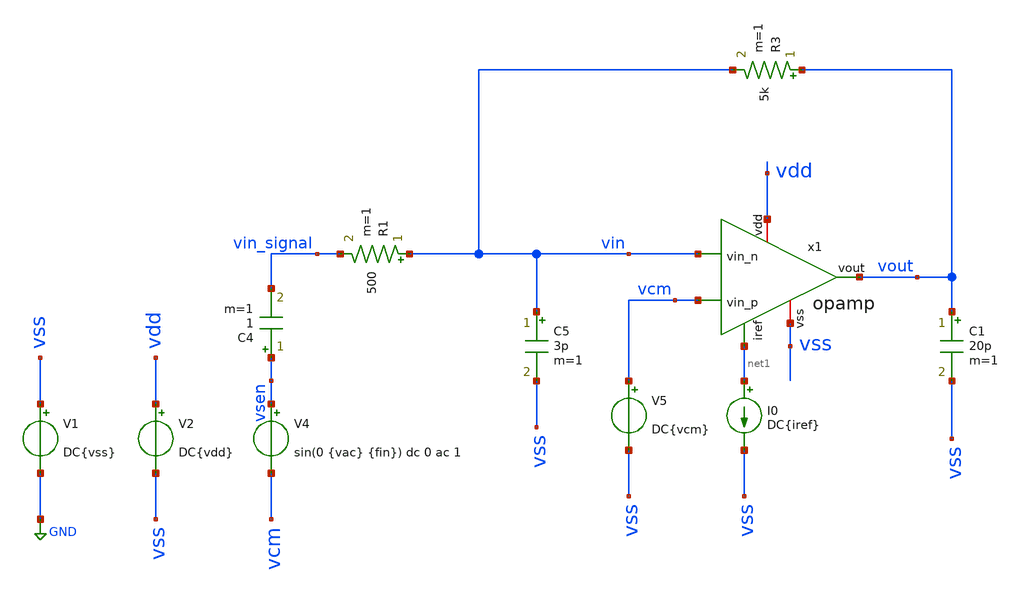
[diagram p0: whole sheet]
** sch_path: TpFinal/Mis Simulaciones/tb_opamp_closeloop.sch
**.subckt tb_opamp_closeloop
V1 vss GND DC{vss}
V2 vdd vss DC{vdd}
V4 vsen vcm sin(0 {vac} {fin}) dc 0 ac 1
C4 vsen vin_signal 1 m=1
I0 net1 vss DC{iref}
R1 vin vin_signal 500 m=1
R3 vout vin 5k m=1
C5 vin vss 3p m=1
C1 vout vss 20p m=1
V5 vcm vss DC{vcm}
x1 vdd net1 vin vcm vout vss opamp
**** begin user architecture code




* Circuit Parameters
.param iref = 105u
.param vdd  = 1.98
.param vss  = 0.0
.param vcm  = 0.88
.param vac  = 10m
.param fin  = 9.765625e5
.options TEMP = 0.0

* FFT Parameters
.param Ts_FFT     = 1e-9
.csparam Ts_FFT   = {Ts_FFT}
.param fin_approx = 1e6
.param NFFT       = 4096
.csparam NFFT     = {NFFT}
.param vac_fin    = 'floor(fin_approx*Ts_FFT*NFFT)/Ts_FFT/NFFT'
.csparam Ti_FFT   = 3u
.csparam vac_fin  = {vac_fin}

* Include Models
.lib ~/skywater/skywater-pdk/libraries/sky130_fd_pr_ngspice/latest/models/corners/sky130.lib FF

* OP Parameters & Singals to save
.save all  @M.X1.XM1.msky130_fd_pr__pfet_01v8_lvt[id] @M.X1.XM1.msky130_fd_pr__pfet_01v8_lvt[vth] @M.X1.XM1.msky130_fd_pr__pfet_01v8_lvt[vgs] @M.X1.XM1.msky130_fd_pr__pfet_01v8_lvt[vds] @M.X1.XM1.msky130_fd_pr__pfet_01v8_lvt[vdsat] @M.X1.XM1.msky130_fd_pr__pfet_01v8_lvt[gm] @M.X1.XM1.msky130_fd_pr__pfet_01v8_lvt[gds] @M.X1.XM1.msky130_fd_pr__pfet_01v8_lvt[cgg]  @M.X1.XM2.msky130_fd_pr__pfet_01v8_lvt[id] @M.X1.XM2.msky130_fd_pr__pfet_01v8_lvt[vth] @M.X1.XM2.msky130_fd_pr__pfet_01v8_lvt[vgs] @M.X1.XM2.msky130_fd_pr__pfet_01v8_lvt[vds] @M.X1.XM2.msky130_fd_pr__pfet_01v8_lvt[vdsat] @M.X1.XM2.msky130_fd_pr__pfet_01v8_lvt[gm] @M.X1.XM2.msky130_fd_pr__pfet_01v8_lvt[gds] @M.X1.XM2.msky130_fd_pr__pfet_01v8_lvt[cgg]  @M.X1.XM3.msky130_fd_pr__nfet_01v8[id] @M.X1.XM3.msky130_fd_pr__nfet_01v8[vth] @M.X1.XM3.msky130_fd_pr__nfet_01v8[vgs] @M.X1.XM3.msky130_fd_pr__nfet_01v8[vds] @M.X1.XM3.msky130_fd_pr__nfet_01v8[vdsat] @M.X1.XM3.msky130_fd_pr__nfet_01v8[gm] @M.X1.XM3.msky130_fd_pr__nfet_01v8[gds]  @M.X1.XM4.msky130_fd_pr__nfet_01v8[id] @M.X1.XM4.msky130_fd_pr__nfet_01v8[vth] @M.X1.XM4.msky130_fd_pr__nfet_01v8[vgs] @M.X1.XM4.msky130_fd_pr__nfet_01v8[vds] @M.X1.XM4.msky130_fd_pr__nfet_01v8[vdsat] @M.X1.XM4.msky130_fd_pr__nfet_01v8[gm] @M.X1.XM4.msky130_fd_pr__nfet_01v8[gds]  @M.X1.XM5.msky130_fd_pr__pfet_01v8[id] @M.X1.XM5.msky130_fd_pr__pfet_01v8[vth] @M.X1.XM5.msky130_fd_pr__pfet_01v8[vgs] @M.X1.XM5.msky130_fd_pr__pfet_01v8[vds] @M.X1.XM5.msky130_fd_pr__pfet_01v8[vdsat] @M.X1.XM5.msky130_fd_pr__pfet_01v8[gm] @M.X1.XM5.msky130_fd_pr__pfet_01v8[gds]  @M.X1.XM6.msky130_fd_pr__nfet_01v8[id] @M.X1.XM6.msky130_fd_pr__nfet_01v8[vth] @M.X1.XM6.msky130_fd_pr__nfet_01v8[vgs] @M.X1.XM6.msky130_fd_pr__nfet_01v8[vds] @M.X1.XM6.msky130_fd_pr__nfet_01v8[vdsat] @M.X1.XM6.msky130_fd_pr__nfet_01v8[gm] @M.X1.XM6.msky130_fd_pr__nfet_01v8[gds]  @M.X1.XM7.msky130_fd_pr__pfet_01v8[id] @M.X1.XM7.msky130_fd_pr__pfet_01v8[vth] @M.X1.XM7.msky130_fd_pr__pfet_01v8[vgs] @M.X1.XM7.msky130_fd_pr__pfet_01v8[vds] @M.X1.XM7.msky130_fd_pr__pfet_01v8[vdsat] @M.X1.XM7.msky130_fd_pr__pfet_01v8[gm] @M.X1.XM7.msky130_fd_pr__pfet_01v8[gds]  @M.X1.XM8.msky130_fd_pr__pfet_01v8[id] @M.X1.XM8.msky130_fd_pr__pfet_01v8[vth] @M.X1.XM8.msky130_fd_pr__pfet_01v8[vgs] @M.X1.XM8.msky130_fd_pr__pfet_01v8[vds] @M.X1.XM8.msky130_fd_pr__pfet_01v8[vdsat] @M.X1.XM8.msky130_fd_pr__pfet_01v8[gm] @M.X1.XM8.msky130_fd_pr__pfet_01v8[gds]  @M.X1.XM9.msky130_fd_pr__nfet_01v8[id] @M.X1.XM9.msky130_fd_pr__nfet_01v8[vth] @M.X1.XM9.msky130_fd_pr__nfet_01v8[vgs] @M.X1.XM9.msky130_fd_pr__nfet_01v8[vds] @M.X1.XM9.msky130_fd_pr__nfet_01v8[vdsat] @M.X1.XM9.msky130_fd_pr__nfet_01v8[gm] @M.X1.XM9.msky130_fd_pr__nfet_01v8[gds]

*Simulation
.control
  set color0 = white

  ac dec 100 1k 10G
  setplot ac1
  meas ac GBW when vdb(vout)=0
  meas ac DCG find vdb(vout) at=1k
  plot vdb(vout) {vp(vout)*180/PI}

  reset
  tran 0.01u 11u
  setplot tran1
  plot v(vsen) v(vout)

  *reset
  *set sqrnoise
  *noise v(vout) V4 dec 100 1k 10G 1
  *let onoise_total_integrado = maximum(sqrt(integ(onoise_spectrum)))
  *print onoise_total_integrado

  reset
  noise v(vout) V4 dec 100 1k 10G 1
  setplot noise1
  plot onoise_spectrum
  setplot noise2
  print inoise_total
  print onoise_total
  print onoise_total.m.x1.xm1.msky130_fd_pr__pfet_01v8_lvt.1overf
  print onoise_total.m.x1.xm1.msky130_fd_pr__pfet_01v8_lvt.id
  print onoise_total.m.x1.xm2.msky130_fd_pr__pfet_01v8_lvt.1overf
  print onoise_total.m.x1.xm2.msky130_fd_pr__pfet_01v8_lvt.id
  print onoise_total.m.x1.xm3.msky130_fd_pr__nfet_01v8.1overf
  print onoise_total.m.x1.xm3.msky130_fd_pr__nfet_01v8.id
  print onoise_total.m.x1.xm4.msky130_fd_pr__nfet_01v8.1overf
  print onoise_total.m.x1.xm4.msky130_fd_pr__nfet_01v8.id
  print onoise_total.m.x1.xm5.msky130_fd_pr__pfet_01v8.1overf
  print onoise_total.m.x1.xm5.msky130_fd_pr__pfet_01v8.id
  print onoise_total.m.x1.xm6.msky130_fd_pr__nfet_01v8.1overf
  print onoise_total.m.x1.xm6.msky130_fd_pr__nfet_01v8.id
  print onoise_total.m.x1.xm7.msky130_fd_pr__pfet_01v8.1overf
  print onoise_total.m.x1.xm7.msky130_fd_pr__pfet_01v8.id
  vprint onoise_total.m.x1.xm8.msky130_fd_pr__pfet_01v8.1overf
  print onoise_total.m.x1.xm8.msky130_fd_pr__pfet_01v8.id
  set filetype=ascii
  write tpfinal_noise.raw

  reset
  set sqrnoise
  noise v(vout) V4 dec 100 1k 10G 1
  setplot noise3
  plot onoise_spectrum
  plot sqrt(integ(onoise_spectrum))
  let onoise_total_integrado = maximum(sqrt(integ(onoise_spectrum)))
  print onoise_total_integrado

  reset
  tran 0.001u 11u
  fourier 9.765625e5 vout
  let THD_db = db(fourier11[1][3]/fourier11[1][1])
  print THD_db
  let lin-tstart = {Ti_FFT} $ skip the start - up phase
  let lin-tstep = {Ts_FFT}
  let lin-tstop = {Ti_FFT + (NFFT-1) * Ts_FFT} $ end earlier
  linearize vout
  set specwindow = none
  fft vout
  *plot mag(vout)
  plot db(mag(vout)) xlimit 0 20e6

  reset
  op
  setplot op1
  unset filetype
  write tb_opamp_closeloop.raw
.endc

.end


**** end user architecture code
**.ends

* expanding   symbol:  opamp.sym # of pins=6
** sym_path: opamp.sym
** sch_path: opamp.sch
.subckt opamp vdd iref vin_n vin_p vout vss
*.iopin vdd
*.iopin vss
*.ipin vin_n
*.ipin vin_p
*.ipin iref
*.opin vout
XM3 vbn vbn vss vss sky130_fd_pr__nfet_01v8 L=3.6 W=40 nf=1 ad='W * 0.29' as='W * 0.29' pd='2 * (W + 0.29)'
+ ps='2 * (W + 0.29)' nrd='0.29 / W' nrs='0.29 / W' sa=0 sb=0 sd=0 mult=17 m=17
XM4 voe1 vbn vss vss sky130_fd_pr__nfet_01v8 L=3.6 W=40 nf=1 ad='W * 0.29' as='W * 0.29' pd='2 * (W + 0.29)'
+ ps='2 * (W + 0.29)' nrd='0.29 / W' nrs='0.29 / W' sa=0 sb=0 sd=0 mult=17 m=17
XM5 vp iref vdd vdd sky130_fd_pr__pfet_01v8 L=0.8 W=60 nf=1 ad='W * 0.29' as='W * 0.29' pd='2 * (W + 0.29)'
+ ps='2 * (W + 0.29)' nrd='0.29 / W' nrs='0.29 / W' sa=0 sb=0 sd=0 mult=54 m=54
XM7 vout iref vdd vdd sky130_fd_pr__pfet_01v8 L=0.8 W=60 nf=1 ad='W * 0.29' as='W * 0.29' pd='2 * (W + 0.29)'
+ ps='2 * (W + 0.29)' nrd='0.29 / W' nrs='0.29 / W' sa=0 sb=0 sd=0 mult=68 m=68
XM8 iref iref vdd vdd sky130_fd_pr__pfet_01v8 L=0.8 W=60 nf=1 ad='W * 0.29' as='W * 0.29' pd='2 * (W + 0.29)'
+ ps='2 * (W + 0.29)' nrd='0.29 / W' nrs='0.29 / W' sa=0 sb=0 sd=0 mult=5 m=5
XM9 net1 vdd voe1 vss sky130_fd_pr__nfet_01v8 L=0.15 W=8.1 nf=1 ad='W * 0.29' as='W * 0.29' pd='2 * (W + 0.29)'
+ ps='2 * (W + 0.29)' nrd='0.29 / W' nrs='0.29 / W' sa=0 sb=0 sd=0 mult=1 m=1
XM6 vout voe1 vss vss sky130_fd_pr__nfet_01v8 L=0.16 W=82 nf=1 ad='W * 0.29' as='W * 0.29' pd='2 * (W + 0.29)'
+ ps='2 * (W + 0.29)' nrd='0.29 / W' nrs='0.29 / W' sa=0 sb=0 sd=0 mult=14 m=14
XM1 vbn vin_n vp vp sky130_fd_pr__pfet_01v8_lvt L=0.5 W=45 nf=1 ad='int((nf+1)/2) * W/nf * 0.29' as='int((nf+2)/2) * W/nf * 0.29'
+ pd='2*int((nf+1)/2) * (W/nf + 0.29)' ps='2*int((nf+2)/2) * (W/nf + 0.29)' nrd='0.29 / W' nrs='0.29 / W'
+ sa=0 sb=0 sd=0 mult=20 m=20
XM2 voe1 vin_p vp vp sky130_fd_pr__pfet_01v8_lvt L=0.5 W=45 nf=1 ad='int((nf+1)/2) * W/nf * 0.29' as='int((nf+2)/2) * W/nf * 0.29'
+ pd='2*int((nf+1)/2) * (W/nf + 0.29)' ps='2*int((nf+2)/2) * (W/nf + 0.29)' nrd='0.29 / W' nrs='0.29 / W'
+ sa=0 sb=0 sd=0 mult=20 m=20
C1 net1 vout 9.5p m=1
.ends

.GLOBAL GND
.end
